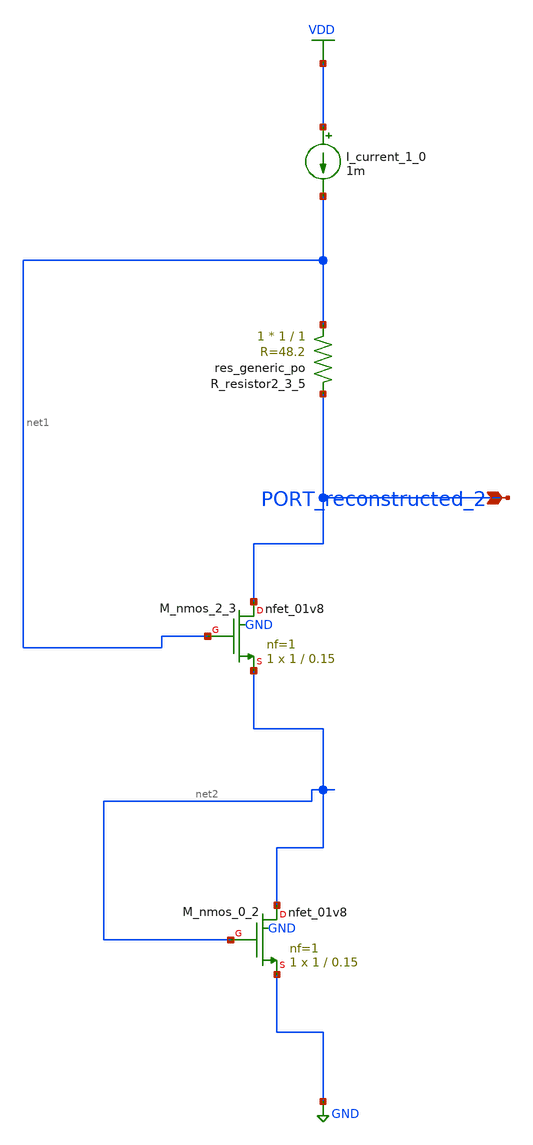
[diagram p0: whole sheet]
** sch_path: schematics/AMSNet/262.sch
**.subckt 262 PORT_reconstructed_2
*.ipin PORT_reconstructed_2
I_current_1_0 VDD net1 1m
XM_nmos_0_2 net2 net2 GND GND sky130_fd_pr__nfet_01v8 L=0.15 W=1 nf=1 ad='int((1 + 1)/2) * 1 / 1 * 0.29'
+ as='int((1 + 2)/2) * 1 / 1 * 0.29' pd='2*int((1 + 1)/2) * (1 / 1 + 0.29)' ps='2*int((1 + 2)/2) * (1 / 1 + 0.29)'
+ nrd='0.29 / 1 ' nrs='0.29 / 1 ' sa=0 sb=0 sd=0 mult=1 m=1
XM_nmos_2_3 PORT_reconstructed_2 net1 net2 GND sky130_fd_pr__nfet_01v8 L=0.15 W=1 nf=1 ad='int((1 + 1)/2) * 1 / 1 * 0.29'
+ as='int((1 + 2)/2) * 1 / 1 * 0.29' pd='2*int((1 + 1)/2) * (1 / 1 + 0.29)' ps='2*int((1 + 2)/2) * (1 / 1 + 0.29)'
+ nrd='0.29 / 1 ' nrs='0.29 / 1 ' sa=0 sb=0 sd=0 mult=1 m=1
XR_resistor2_3_5 net1 PORT_reconstructed_2 sky130_fd_pr__res_generic_po W=1 L=1 m=1
**.ends
.GLOBAL GND
.GLOBAL VDD
.end
